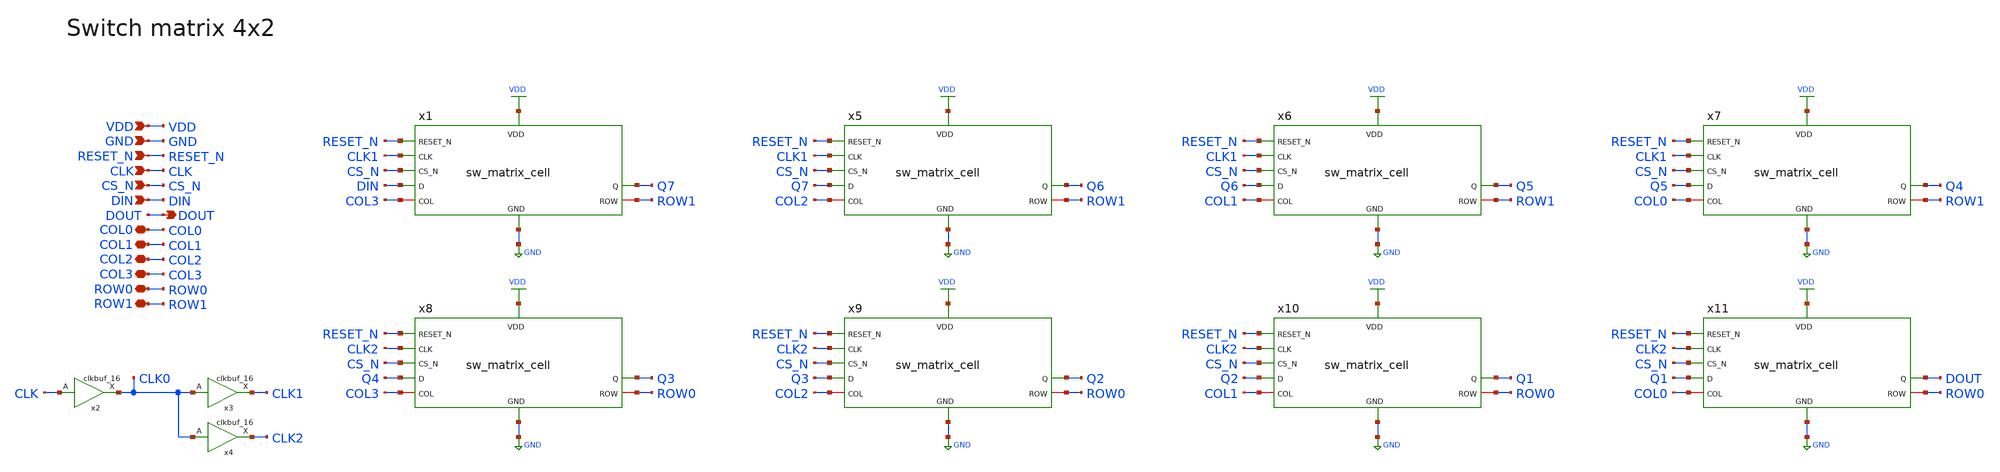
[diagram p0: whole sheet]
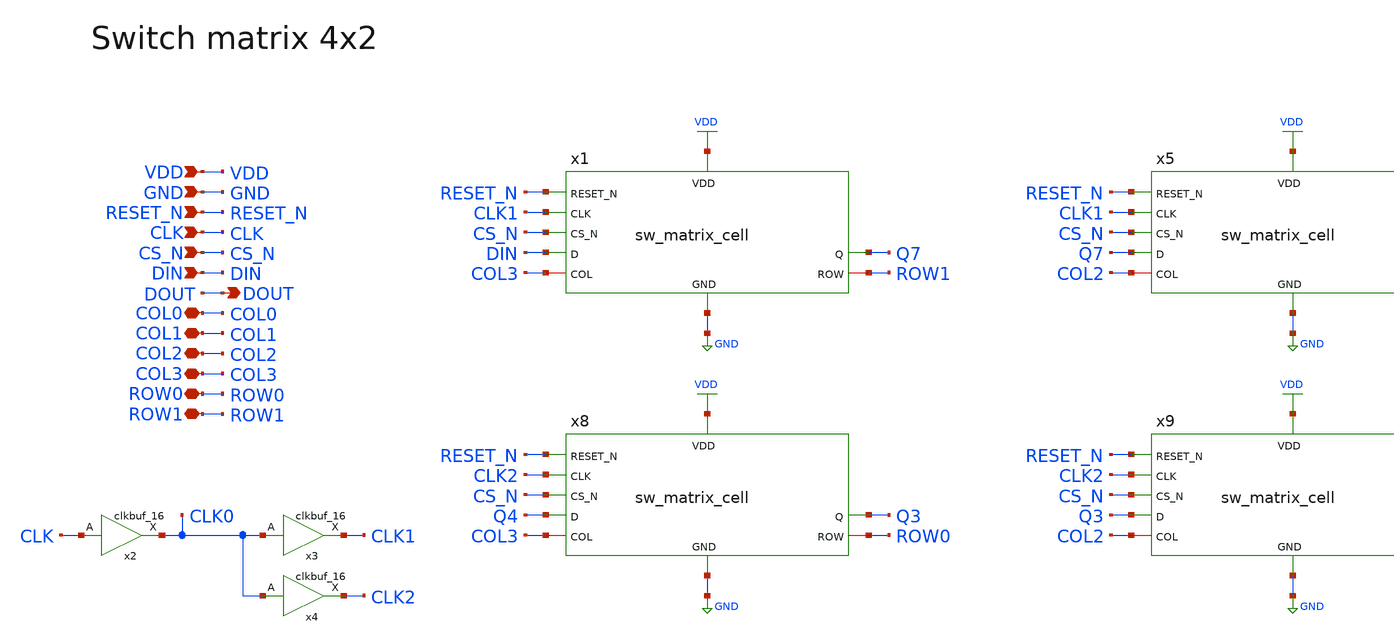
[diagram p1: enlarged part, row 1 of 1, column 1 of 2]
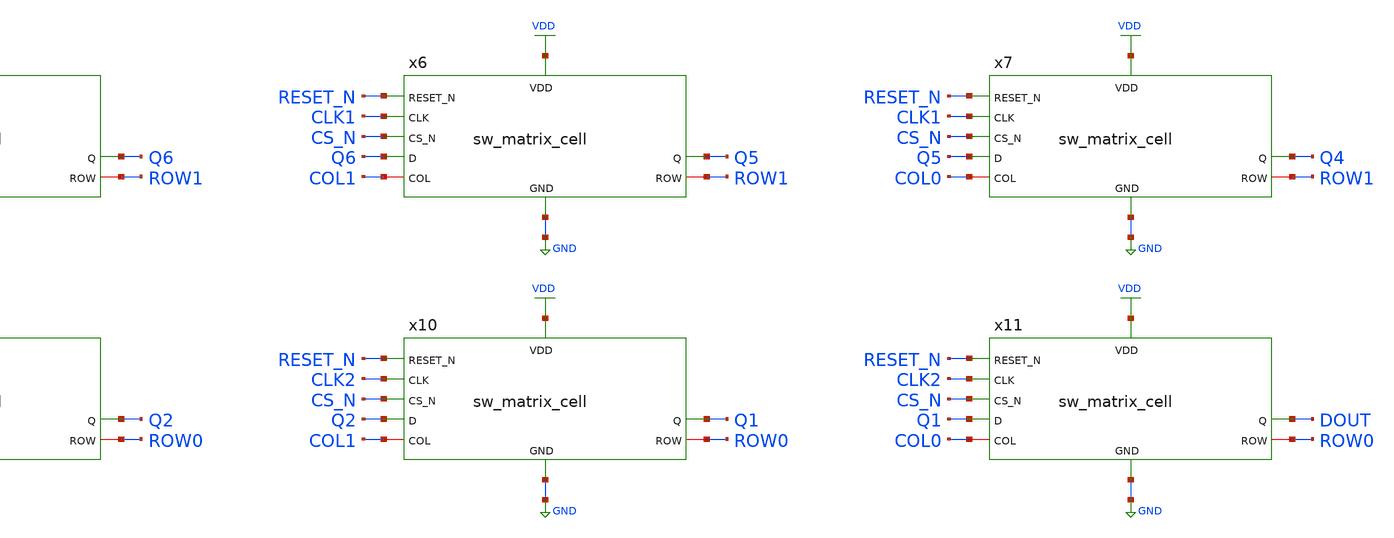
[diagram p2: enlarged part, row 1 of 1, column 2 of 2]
** sch_path: designs/libs/core_analog/sw_matrix/sw_matrix_4x2.sch
* Copyright 2022 GlobalFoundries PDK Authors
* Licensed under the Apache License, Version 2.0 (the "License");
* you may not use this file except in compliance with the License.
* You may obtain a copy of the License at
* https://www.apache.org/licenses/LICENSE-2.0
* Unless required by applicable law or agreed to in writing, software
* distributed under the License is distributed on an "AS IS" BASIS,
* WITHOUT WARRANTIES OR CONDITIONS OF ANY KIND, either express or implied.
* See the License for the specific language governing permissions and
* limitations under the License.
**.subckt sw_matrix_4x2 VDD GND RESET_N CLK CS_N DIN COL0 COL1 COL2 COL3 ROW0 ROW1 DOUT
*.ipin VDD
*.ipin GND
*.ipin RESET_N
*.ipin CLK
*.ipin CS_N
*.ipin DIN
*.iopin COL0
*.iopin COL1
*.iopin COL2
*.iopin COL3
*.iopin ROW0
*.iopin ROW1
*.opin DOUT
x1 VDD GND RESET_N CLK1 DIN CS_N Q7 COL3 ROW1 sw_matrix_cell
x5 VDD GND RESET_N CLK1 Q7 CS_N Q6 COL2 ROW1 sw_matrix_cell
x6 VDD GND RESET_N CLK1 Q6 CS_N Q5 COL1 ROW1 sw_matrix_cell
x7 VDD GND RESET_N CLK1 Q5 CS_N Q4 COL0 ROW1 sw_matrix_cell
x8 VDD GND RESET_N CLK2 Q4 CS_N Q3 COL3 ROW0 sw_matrix_cell
x9 VDD GND RESET_N CLK2 Q3 CS_N Q2 COL2 ROW0 sw_matrix_cell
x10 VDD GND RESET_N CLK2 Q2 CS_N Q1 COL1 ROW0 sw_matrix_cell
x11 VDD GND RESET_N CLK2 Q1 CS_N DOUT COL0 ROW0 sw_matrix_cell
x2 CLK CLK0 VDD VDD GND GND gf180mcu_fd_sc_mcu7t5v0__clkbuf_16
x3 CLK0 CLK1 VDD VDD GND GND gf180mcu_fd_sc_mcu7t5v0__clkbuf_16
x4 CLK0 CLK2 VDD VDD GND GND gf180mcu_fd_sc_mcu7t5v0__clkbuf_16
**.ends
.GLOBAL GND
.GLOBAL VDD
.end
